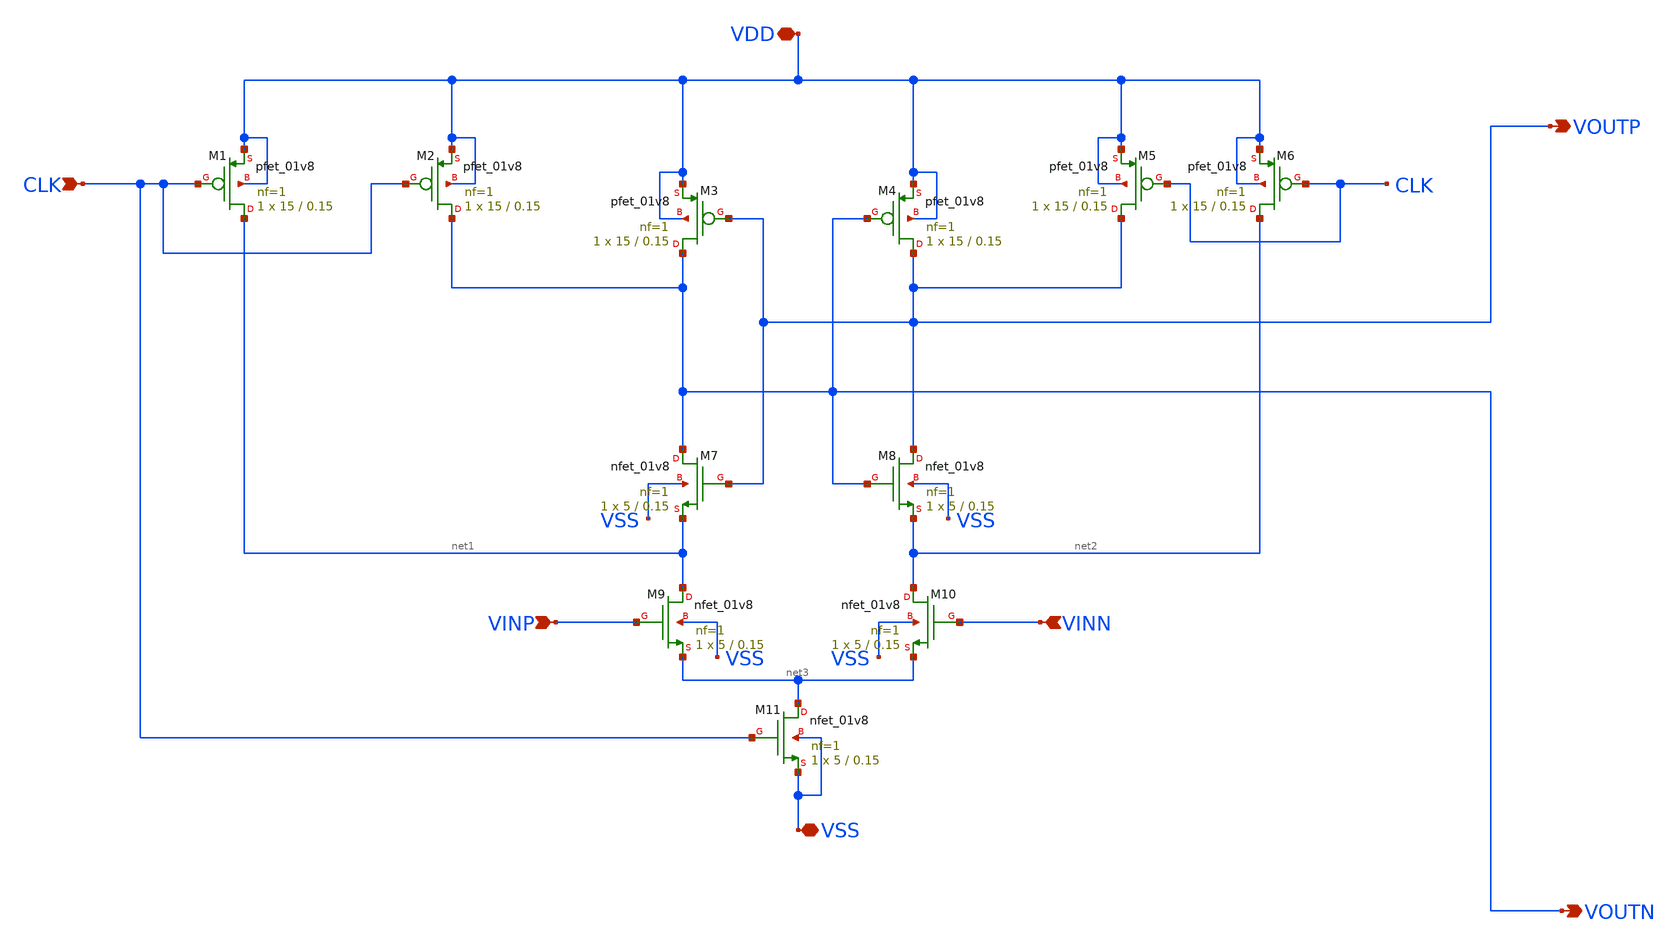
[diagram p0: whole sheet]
** sch_path: SKY130/SAR-ADC/SAR-ADC_1.8V/comp_arm_min.sch
**.subckt comp_arm_min VSS VDD CLK VINP VINN VOUTN VOUTP
*.iopin VSS
*.iopin VDD
*.ipin CLK
*.ipin VINP
*.ipin VINN
*.opin VOUTN
*.opin VOUTP
XM1 net1 CLK VDD VDD sky130_fd_pr__pfet_01v8 L=0.15 W=15 nf=1 ad='int((1 + 1)/2) * 15 / 1 * 0.29' as='int((1 + 2)/2) * 15 / 1 * 0.29'
+ pd='2*int((1 + 1)/2) * (15 / 1 + 0.29)' ps='2*int((1 + 2)/2) * (15 / 1 + 0.29)' nrd='0.29 / 15 ' nrs='0.29 / 15 '
+ sa=0 sb=0 sd=0 mult=1 m=1
XM2 VOUTN CLK VDD VDD sky130_fd_pr__pfet_01v8 L=0.15 W=15 nf=1 ad='int((1 + 1)/2) * 15 / 1 * 0.29' as='int((1 + 2)/2) * 15 / 1 * 0.29'
+ pd='2*int((1 + 1)/2) * (15 / 1 + 0.29)' ps='2*int((1 + 2)/2) * (15 / 1 + 0.29)' nrd='0.29 / 15 ' nrs='0.29 / 15 '
+ sa=0 sb=0 sd=0 mult=1 m=1
XM3 VOUTN VOUTP VDD VDD sky130_fd_pr__pfet_01v8 L=0.15 W=15 nf=1 ad='int((1 + 1)/2) * 15 / 1 * 0.29'
+ as='int((1 + 2)/2) * 15 / 1 * 0.29' pd='2*int((1 + 1)/2) * (15 / 1 + 0.29)' ps='2*int((1 + 2)/2) * (15 / 1 + 0.29)'
+ nrd='0.29 / 15 ' nrs='0.29 / 15 ' sa=0 sb=0 sd=0 mult=1 m=1
XM4 VOUTP VOUTN VDD VDD sky130_fd_pr__pfet_01v8 L=0.15 W=15 nf=1 ad='int((1 + 1)/2) * 15 / 1 * 0.29'
+ as='int((1 + 2)/2) * 15 / 1 * 0.29' pd='2*int((1 + 1)/2) * (15 / 1 + 0.29)' ps='2*int((1 + 2)/2) * (15 / 1 + 0.29)'
+ nrd='0.29 / 15 ' nrs='0.29 / 15 ' sa=0 sb=0 sd=0 mult=1 m=1
XM5 VOUTP CLK VDD VDD sky130_fd_pr__pfet_01v8 L=0.15 W=15 nf=1 ad='int((1 + 1)/2) * 15 / 1 * 0.29' as='int((1 + 2)/2) * 15 / 1 * 0.29'
+ pd='2*int((1 + 1)/2) * (15 / 1 + 0.29)' ps='2*int((1 + 2)/2) * (15 / 1 + 0.29)' nrd='0.29 / 15 ' nrs='0.29 / 15 '
+ sa=0 sb=0 sd=0 mult=1 m=1
XM6 net2 CLK VDD VDD sky130_fd_pr__pfet_01v8 L=0.15 W=15 nf=1 ad='int((1 + 1)/2) * 15 / 1 * 0.29' as='int((1 + 2)/2) * 15 / 1 * 0.29'
+ pd='2*int((1 + 1)/2) * (15 / 1 + 0.29)' ps='2*int((1 + 2)/2) * (15 / 1 + 0.29)' nrd='0.29 / 15 ' nrs='0.29 / 15 '
+ sa=0 sb=0 sd=0 mult=1 m=1
XM7 VOUTN VOUTP net1 VSS sky130_fd_pr__nfet_01v8 L=0.15 W=5 nf=1 ad='int((1 + 1)/2) * 5 / 1 * 0.29' as='int((1 + 2)/2) * 5 / 1 * 0.29'
+ pd='2*int((1 + 1)/2) * (5 / 1 + 0.29)' ps='2*int((1 + 2)/2) * (5 / 1 + 0.29)' nrd='0.29 / 5 ' nrs='0.29 / 5 '
+ sa=0 sb=0 sd=0 mult=1 m=1
XM10 net2 VINN net3 VSS sky130_fd_pr__nfet_01v8 L=0.15 W=5 nf=1 ad='int((1 + 1)/2) * 5 / 1 * 0.29' as='int((1 + 2)/2) * 5 / 1 * 0.29'
+ pd='2*int((1 + 1)/2) * (5 / 1 + 0.29)' ps='2*int((1 + 2)/2) * (5 / 1 + 0.29)' nrd='0.29 / 5 ' nrs='0.29 / 5 '
+ sa=0 sb=0 sd=0 mult=1 m=1
XM8 VOUTP VOUTN net2 VSS sky130_fd_pr__nfet_01v8 L=0.15 W=5 nf=1 ad='int((1 + 1)/2) * 5 / 1 * 0.29' as='int((1 + 2)/2) * 5 / 1 * 0.29'
+ pd='2*int((1 + 1)/2) * (5 / 1 + 0.29)' ps='2*int((1 + 2)/2) * (5 / 1 + 0.29)' nrd='0.29 / 5 ' nrs='0.29 / 5 '
+ sa=0 sb=0 sd=0 mult=1 m=1
XM9 net1 VINP net3 VSS sky130_fd_pr__nfet_01v8 L=0.15 W=5 nf=1 ad='int((1 + 1)/2) * 5 / 1 * 0.29' as='int((1 + 2)/2) * 5 / 1 * 0.29'
+ pd='2*int((1 + 1)/2) * (5 / 1 + 0.29)' ps='2*int((1 + 2)/2) * (5 / 1 + 0.29)' nrd='0.29 / 5 ' nrs='0.29 / 5 '
+ sa=0 sb=0 sd=0 mult=1 m=1
XM11 net3 CLK VSS VSS sky130_fd_pr__nfet_01v8 L=0.15 W=5 nf=1 ad='int((1 + 1)/2) * 5 / 1 * 0.29' as='int((1 + 2)/2) * 5 / 1 * 0.29'
+ pd='2*int((1 + 1)/2) * (5 / 1 + 0.29)' ps='2*int((1 + 2)/2) * (5 / 1 + 0.29)' nrd='0.29 / 5 ' nrs='0.29 / 5 '
+ sa=0 sb=0 sd=0 mult=1 m=1
**.ends
.end
